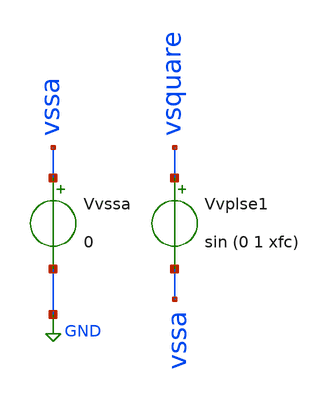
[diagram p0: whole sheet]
** sch_path: fft_analysis/tb_fft.sch
**.subckt tb_fft
Vvssa vssa GND 0
Vvplse1 vsquare vssa sin (0 1 xfc)
**** begin user architecture code

* Parameters
.param xVsq = 1
.param xtr = 20p
.param xtf = 20p
*.param xfc = 1.00006103515625e6
.param xfc = 1.0546875e6
*.param xTc = 1u
.param xTc = 1/xfc
.param xtpw = (xTc/2)-xtr
*.param xtpw = 0.5u
.param numPeriods = 40
*.csparam xtsim = {numPeriods*xT}
*.csparam xtsim = 106u
.csparam xtsim = 26.6u
*.csparam xtsim = 20u
  .control

  save all
  echo $&xtsim

** 1. TRAN SIM **

  tran 1n $&xtsim

  set xbrushwidth=2         ; assign value 2 to the predefined variable
  *plot tran1.v(vsquare)
  print v(vsquare) > vsquare_nonlin_data.txt
  remzerovec
  write tb_OTA_tran1.raw

** 2. LINEARISATION **

  let lin-tstart = 1u
*  let lin-tstop = 103.4u-((1/40Meg)*0)
  *let lin-tstop = 230.456u
  * coherant sampling
  *let lin-tstop = 3277.8u-((1/40Meg)*1)
  * non-coherant sampling
  *let lin-tstop = 3277.55u-((1/40Meg)*0)
   * nlow res coherant sampling
  *let lin-tstop = 26.6u-((1/40Meg)*1)
  * nlow res coherant sampling
  let lin-tstop = 26.6u-((1/40Meg)*1)-0.25u
  *let lin-tstop = 100u
  echo $&lin-tstop
  * 40Meg
  let lin-fs = 40Meg
  let lin-tstep = 1/40Meg
  linearize v(vsquare)
  remzerovec
  write tb_OTA_tran2.raw
  print v(vsquare) > vsquare_lin_data.txt

** 3. FFT (none) **

  set specwindow = none
  *set specwindow = rectangular
  *set specwindow = bartlet
  *set specwindow = blackman
  *set specwindow = hanning
  *set specwindow = gaussian
  *set specwindow = flattop

  *spec 0 20Meg 9.765625e3 v(vsquare)
  fft v(vsquare)
  print v(vsquare) > vsquare_fft_data_none.txt
  plot 20*log10(mag(1*v(vsquare)))
  remzerovec
  write tb_OTA_sp2.raw

  ** 4. FFT (rectangular) **
  setplot tran2
  *set specwindow = none
  set specwindow = rectangular
  *set specwindow = bartlet
  *set specwindow = blackman
  *set specwindow = hanning
  *set specwindow = gaussian
  *set specwindow = flattop

  *spec 0 20Meg 9.765625e3 v(vsquare)
  fft v(vsquare)
  print v(vsquare) > vsquare_fft_data_rec.txt
  *plot 20*log10(mag(1*v(vsquare)))
  remzerovec
  write tb_OTA_sp3.raw

   ** 5. FFT (bartlet) **
  setplot tran2
  *set specwindow = none
  *set specwindow = rectangular
  set specwindow = bartlet
  *set specwindow = blackman
  *set specwindow = hanning
  *set specwindow = gaussian
  *set specwindow = flattop

  *spec 0 20Meg 9.765625e3 v(vsquare)
  fft v(vsquare)
  print v(vsquare) > vsquare_fft_data_bart.txt
  *plot 20*log10(mag(1*v(vsquare)))
  remzerovec
  write tb_OTA_sp4.raw

  ** 6. FFT (blackman) **
  setplot tran2
  *set specwindow = none
  *set specwindow = rectangular
  *set specwindow = bartlet
  set specwindow = blackman
  *set specwindow = hanning
  *set specwindow = gaussian
  *set specwindow = flattop

  *spec 0 20Meg 9.765625e3 v(vsquare)
  fft v(vsquare)
  print v(vsquare) > vsquare_fft_data_black.txt
  *plot 20*log10(mag(1*v(vsquare)))
  remzerovec
  write tb_OTA_sp5.raw

  ** 7. FFT (hanning) **
  setplot tran2
  *set specwindow = none
  *set specwindow = rectangular
  *set specwindow = bartlet
  *set specwindow = blackmanharris
  set specwindow = hanning
  *set specwindow = gaussian
  *set specwindow = flattop

  *spec 0 20Meg 9.765625e3 v(vsquare)
  fft v(vsquare)
  print v(vsquare) > vsquare_fft_data_hann.txt
  *plot 20*log10(mag(1*v(vsquare)))
  remzerovec
  write tb_OTA_sp6.raw

  ** 8 FFT (gaussian) **
  setplot tran2
  *set specwindow = none
  *set specwindow = rectangular
  *set specwindow = bartlet
  *set specwindow = blackman
  *set specwindow = hanning
  set specwindow = gaussian
  *set specwindow = flattop

  *spec 0 20Meg 9.765625e3 v(vsquare)
  fft v(vsquare)
  print v(vsquare) > vsquare_fft_data_gauss.txt
  *plot 20*log10(mag(1*v(vsquare)))
  remzerovec
  write tb_OTA_sp7.raw

   ** 9 FFT (flatop) **
  setplot tran2
  *set specwindow = none
  *set specwindow = rectangular
  *set specwindow = bartlet
  *set specwindow = blackman
  *set specwindow = hanning
  *set specwindow = gaussian
  set specwindow = flattop

  *spec 0 20Meg 9.765625e3 v(vsquare)
  fft v(vsquare)
  print v(vsquare) > vsquare_fft_data_flat.txt
  *plot 20*log10(mag(1*v(vsquare)))
  remzerovec
  write tb_OTA_sp8.raw

   ** 10 FFT (blackman harris) **
  setplot tran2
  *set specwindow = none
  *set specwindow = rectangular
  *set specwindow = bartlet
  set specwindow = blackmanharris
  *set specwindow = hanning
  *set specwindow = gaussian
  *set specwindow = flattop

  *spec 0 20Meg 9.765625e3 v(vsquare)
  fft v(vsquare)
  print v(vsquare) > vsquare_fft_data_blackmanharris.txt
  *plot 20*log10(mag(1*v(vsquare)))
  remzerovec
  write tb_OTA_sp8.raw


  setplot

.endc




**** end user architecture code
**.ends
.GLOBAL GND
.end
